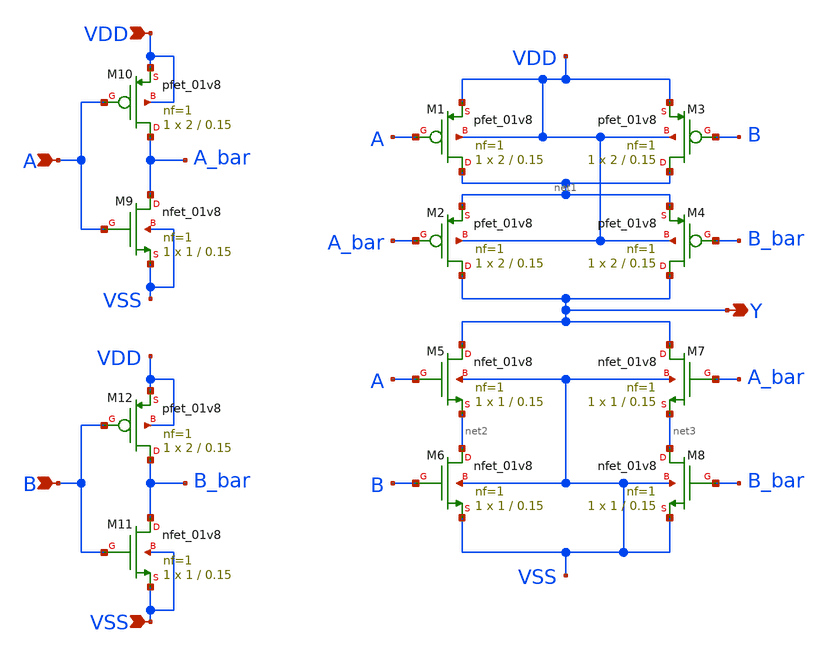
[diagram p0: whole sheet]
** sch_path: xor.sch
**.subckt xor A VDD Y B VSS
*.ipin A
*.ipin VDD
*.opin Y
*.ipin B
*.ipin VSS
XM1 net1 A VDD VDD sky130_fd_pr__pfet_01v8 L=0.15 W=2 nf=1 ad='int((nf+1)/2) * W/nf * 0.29' as='int((nf+2)/2) * W/nf * 0.29'
+ pd='2*int((nf+1)/2) * (W/nf + 0.29)' ps='2*int((nf+2)/2) * (W/nf + 0.29)' nrd='0.29 / W' nrs='0.29 / W'
+ sa=0 sb=0 sd=0 mult=1 m=1
XM2 Y A_bar net1 VDD sky130_fd_pr__pfet_01v8 L=0.15 W=2 nf=1 ad='int((nf+1)/2) * W/nf * 0.29' as='int((nf+2)/2) * W/nf * 0.29'
+ pd='2*int((nf+1)/2) * (W/nf + 0.29)' ps='2*int((nf+2)/2) * (W/nf + 0.29)' nrd='0.29 / W' nrs='0.29 / W'
+ sa=0 sb=0 sd=0 mult=1 m=1
XM3 net1 B VDD VDD sky130_fd_pr__pfet_01v8 L=0.15 W=2 nf=1 ad='int((nf+1)/2) * W/nf * 0.29' as='int((nf+2)/2) * W/nf * 0.29'
+ pd='2*int((nf+1)/2) * (W/nf + 0.29)' ps='2*int((nf+2)/2) * (W/nf + 0.29)' nrd='0.29 / W' nrs='0.29 / W'
+ sa=0 sb=0 sd=0 mult=1 m=1
XM4 Y B_bar net1 VDD sky130_fd_pr__pfet_01v8 L=0.15 W=2 nf=1 ad='int((nf+1)/2) * W/nf * 0.29' as='int((nf+2)/2) * W/nf * 0.29'
+ pd='2*int((nf+1)/2) * (W/nf + 0.29)' ps='2*int((nf+2)/2) * (W/nf + 0.29)' nrd='0.29 / W' nrs='0.29 / W'
+ sa=0 sb=0 sd=0 mult=1 m=1
XM5 Y A net2 VSS sky130_fd_pr__nfet_01v8 L=0.15 W=1 nf=1 ad='int((nf+1)/2) * W/nf * 0.29' as='int((nf+2)/2) * W/nf * 0.29'
+ pd='2*int((nf+1)/2) * (W/nf + 0.29)' ps='2*int((nf+2)/2) * (W/nf + 0.29)' nrd='0.29 / W' nrs='0.29 / W'
+ sa=0 sb=0 sd=0 mult=1 m=1
XM6 net2 B VSS VSS sky130_fd_pr__nfet_01v8 L=0.15 W=1 nf=1 ad='int((nf+1)/2) * W/nf * 0.29' as='int((nf+2)/2) * W/nf * 0.29'
+ pd='2*int((nf+1)/2) * (W/nf + 0.29)' ps='2*int((nf+2)/2) * (W/nf + 0.29)' nrd='0.29 / W' nrs='0.29 / W'
+ sa=0 sb=0 sd=0 mult=1 m=1
XM7 Y A_bar net3 VSS sky130_fd_pr__nfet_01v8 L=0.15 W=1 nf=1 ad='int((nf+1)/2) * W/nf * 0.29' as='int((nf+2)/2) * W/nf * 0.29'
+ pd='2*int((nf+1)/2) * (W/nf + 0.29)' ps='2*int((nf+2)/2) * (W/nf + 0.29)' nrd='0.29 / W' nrs='0.29 / W'
+ sa=0 sb=0 sd=0 mult=1 m=1
XM8 net3 B_bar VSS VSS sky130_fd_pr__nfet_01v8 L=0.15 W=1 nf=1 ad='int((nf+1)/2) * W/nf * 0.29' as='int((nf+2)/2) * W/nf * 0.29'
+ pd='2*int((nf+1)/2) * (W/nf + 0.29)' ps='2*int((nf+2)/2) * (W/nf + 0.29)' nrd='0.29 / W' nrs='0.29 / W'
+ sa=0 sb=0 sd=0 mult=1 m=1
XM9 A_bar A VSS VSS sky130_fd_pr__nfet_01v8 L=0.15 W=1 nf=1 ad='int((nf+1)/2) * W/nf * 0.29' as='int((nf+2)/2) * W/nf * 0.29'
+ pd='2*int((nf+1)/2) * (W/nf + 0.29)' ps='2*int((nf+2)/2) * (W/nf + 0.29)' nrd='0.29 / W' nrs='0.29 / W'
+ sa=0 sb=0 sd=0 mult=1 m=1
XM10 A_bar A VDD VDD sky130_fd_pr__pfet_01v8 L=0.15 W=2 nf=1 ad='int((nf+1)/2) * W/nf * 0.29' as='int((nf+2)/2) * W/nf * 0.29'
+ pd='2*int((nf+1)/2) * (W/nf + 0.29)' ps='2*int((nf+2)/2) * (W/nf + 0.29)' nrd='0.29 / W' nrs='0.29 / W'
+ sa=0 sb=0 sd=0 mult=1 m=1
XM11 B_bar B VSS VSS sky130_fd_pr__nfet_01v8 L=0.15 W=1 nf=1 ad='int((nf+1)/2) * W/nf * 0.29' as='int((nf+2)/2) * W/nf * 0.29'
+ pd='2*int((nf+1)/2) * (W/nf + 0.29)' ps='2*int((nf+2)/2) * (W/nf + 0.29)' nrd='0.29 / W' nrs='0.29 / W'
+ sa=0 sb=0 sd=0 mult=1 m=1
XM12 B_bar B VDD VDD sky130_fd_pr__pfet_01v8 L=0.15 W=2 nf=1 ad='int((nf+1)/2) * W/nf * 0.29' as='int((nf+2)/2) * W/nf * 0.29'
+ pd='2*int((nf+1)/2) * (W/nf + 0.29)' ps='2*int((nf+2)/2) * (W/nf + 0.29)' nrd='0.29 / W' nrs='0.29 / W'
+ sa=0 sb=0 sd=0 mult=1 m=1
**.ends
.end
